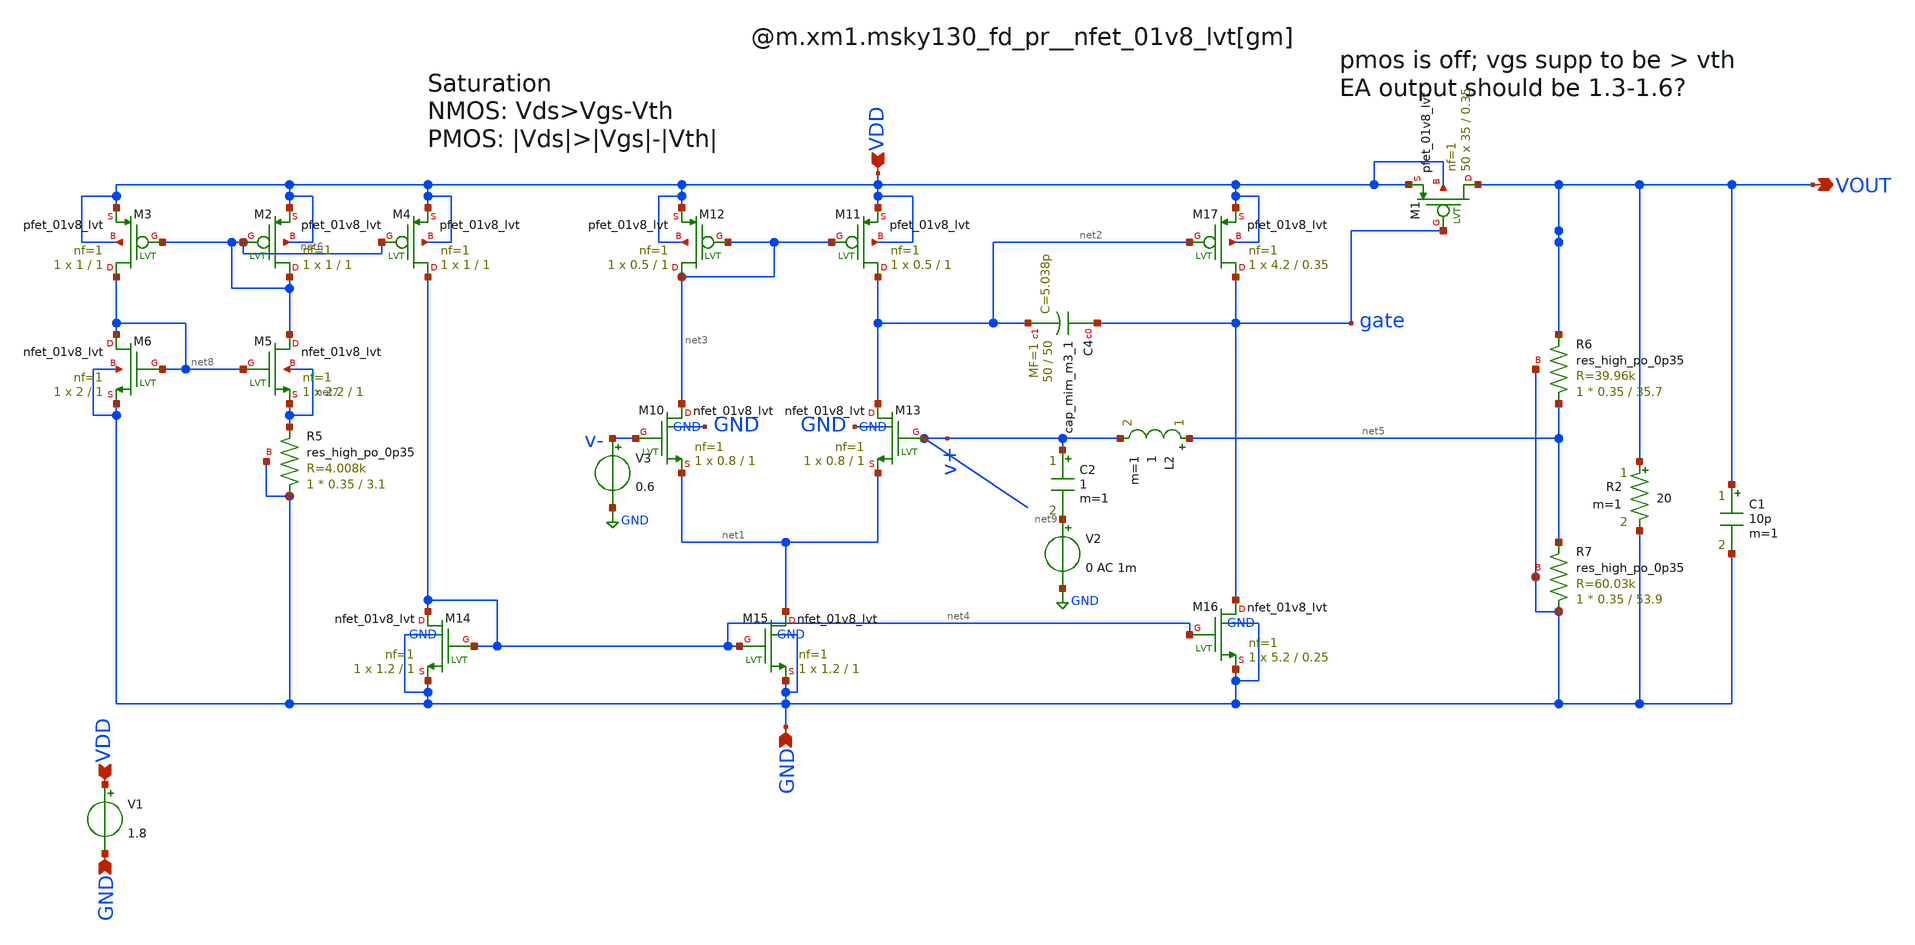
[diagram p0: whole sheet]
** sch_path: xschem/testbenches/FreqResponse-v4.sch
**.subckt FreqResponse-v4 VDD VOUT GND VDD GND
*.ipin VDD
*.opin VOUT
*.ipin GND
*.ipin VDD
*.ipin GND
V3 v- GND 0.6
XM10 net3 v- net1 GND sky130_fd_pr__nfet_01v8_lvt L=1 W=0.8 nf=1 ad='int((1 + 1)/2) * 0.8 / 1 * 0.29'
+ as='int((1 + 2)/2) * 0.8 / 1 * 0.29' pd='2*int((1 + 1)/2) * (0.8 / 1 + 0.29)' ps='2*int((1 + 2)/2) * (0.8 / 1 + 0.29)'
+ nrd='0.29 / 0.8 ' nrs='0.29 / 0.8 ' sa=0 sb=0 sd=0 mult=1 m=1
XM11 net2 net3 VDD VDD sky130_fd_pr__pfet_01v8_lvt L=1 W=0.5 nf=1 ad='int((1 + 1)/2) * 0.5 / 1 * 0.29'
+ as='int((1 + 2)/2) * 0.5 / 1 * 0.29' pd='2*int((1 + 1)/2) * (0.5 / 1 + 0.29)' ps='2*int((1 + 2)/2) * (0.5 / 1 + 0.29)'
+ nrd='0.29 / 0.5 ' nrs='0.29 / 0.5 ' sa=0 sb=0 sd=0 mult=1 m=1
XM12 net3 net3 VDD VDD sky130_fd_pr__pfet_01v8_lvt L=1 W=0.5 nf=1 ad='int((1 + 1)/2) * 0.5 / 1 * 0.29'
+ as='int((1 + 2)/2) * 0.5 / 1 * 0.29' pd='2*int((1 + 1)/2) * (0.5 / 1 + 0.29)' ps='2*int((1 + 2)/2) * (0.5 / 1 + 0.29)'
+ nrd='0.29 / 0.5 ' nrs='0.29 / 0.5 ' sa=0 sb=0 sd=0 mult=1 m=1
XM13 net2 v+ net1 GND sky130_fd_pr__nfet_01v8_lvt L=1 W=0.8 nf=1 ad='int((1 + 1)/2) * 0.8 / 1 * 0.29'
+ as='int((1 + 2)/2) * 0.8 / 1 * 0.29' pd='2*int((1 + 1)/2) * (0.8 / 1 + 0.29)' ps='2*int((1 + 2)/2) * (0.8 / 1 + 0.29)'
+ nrd='0.29 / 0.8 ' nrs='0.29 / 0.8 ' sa=0 sb=0 sd=0 mult=1 m=1
XM14 net4 net4 GND GND sky130_fd_pr__nfet_01v8_lvt L=1 W=1.2 nf=1 ad='int((1 + 1)/2) * 1.2 / 1 * 0.29'
+ as='int((1 + 2)/2) * 1.2 / 1 * 0.29' pd='2*int((1 + 1)/2) * (1.2 / 1 + 0.29)' ps='2*int((1 + 2)/2) * (1.2 / 1 + 0.29)'
+ nrd='0.29 / 1.2 ' nrs='0.29 / 1.2 ' sa=0 sb=0 sd=0 mult=1 m=1
XM15 net1 net4 GND GND sky130_fd_pr__nfet_01v8_lvt L=1 W=1.2 nf=1 ad='int((1 + 1)/2) * 1.2 / 1 * 0.29'
+ as='int((1 + 2)/2) * 1.2 / 1 * 0.29' pd='2*int((1 + 1)/2) * (1.2 / 1 + 0.29)' ps='2*int((1 + 2)/2) * (1.2 / 1 + 0.29)'
+ nrd='0.29 / 1.2 ' nrs='0.29 / 1.2 ' sa=0 sb=0 sd=0 mult=1 m=1
XM16 gate net4 GND GND sky130_fd_pr__nfet_01v8_lvt L=0.25 W=5.2 nf=1 ad='int((1 + 1)/2) * 5.2 / 1 * 0.29'
+ as='int((1 + 2)/2) * 5.2 / 1 * 0.29' pd='2*int((1 + 1)/2) * (5.2 / 1 + 0.29)' ps='2*int((1 + 2)/2) * (5.2 / 1 + 0.29)'
+ nrd='0.29 / 5.2 ' nrs='0.29 / 5.2 ' sa=0 sb=0 sd=0 mult=1 m=1
XM17 gate net2 VDD VDD sky130_fd_pr__pfet_01v8_lvt L=0.35 W=4.2 nf=1 ad='int((1 + 1)/2) * 4.2 / 1 * 0.29'
+ as='int((1 + 2)/2) * 4.2 / 1 * 0.29' pd='2*int((1 + 1)/2) * (4.2 / 1 + 0.29)' ps='2*int((1 + 2)/2) * (4.2 / 1 + 0.29)'
+ nrd='0.29 / 4.2 ' nrs='0.29 / 4.2 ' sa=0 sb=0 sd=0 mult=1 m=1
XM1 VOUT gate VDD VDD sky130_fd_pr__pfet_01v8_lvt L=0.35 W=35 nf=1 ad='int((1 + 1)/2) * 35 / 1 * 0.29'
+ as='int((1 + 2)/2) * 35 / 1 * 0.29' pd='2*int((1 + 1)/2) * (35 / 1 + 0.29)' ps='2*int((1 + 2)/2) * (35 / 1 + 0.29)'
+ nrd='0.29 / 35 ' nrs='0.29 / 35 ' sa=0 sb=0 sd=0 mult=50 m=50
V1 VDD GND 1.8
V2 net9 GND 0 AC 1m
R2 VOUT GND 20 m=1
C1 VOUT GND 10p m=1
XM2 net6 net6 VDD VDD sky130_fd_pr__pfet_01v8_lvt L=1 W=1 nf=1 ad='int((1 + 1)/2) * 1 / 1 * 0.29' as='int((1 + 2)/2) * 1 / 1 * 0.29'
+ pd='2*int((1 + 1)/2) * (1 / 1 + 0.29)' ps='2*int((1 + 2)/2) * (1 / 1 + 0.29)' nrd='0.29 / 1 ' nrs='0.29 / 1 '
+ sa=0 sb=0 sd=0 mult=1 m=1
XM3 net8 net6 VDD VDD sky130_fd_pr__pfet_01v8_lvt L=1 W=1 nf=1 ad='int((1 + 1)/2) * 1 / 1 * 0.29' as='int((1 + 2)/2) * 1 / 1 * 0.29'
+ pd='2*int((1 + 1)/2) * (1 / 1 + 0.29)' ps='2*int((1 + 2)/2) * (1 / 1 + 0.29)' nrd='0.29 / 1 ' nrs='0.29 / 1 '
+ sa=0 sb=0 sd=0 mult=1 m=1
XM4 net4 net6 VDD VDD sky130_fd_pr__pfet_01v8_lvt L=1 W=1 nf=1 ad='int((1 + 1)/2) * 1 / 1 * 0.29' as='int((1 + 2)/2) * 1 / 1 * 0.29'
+ pd='2*int((1 + 1)/2) * (1 / 1 + 0.29)' ps='2*int((1 + 2)/2) * (1 / 1 + 0.29)' nrd='0.29 / 1 ' nrs='0.29 / 1 '
+ sa=0 sb=0 sd=0 mult=1 m=1
XM5 net6 net8 net7 net7 sky130_fd_pr__nfet_01v8_lvt L=1 W=2.2 nf=1 ad='int((1 + 1)/2) * 2.2 / 1 * 0.29'
+ as='int((1 + 2)/2) * 2.2 / 1 * 0.29' pd='2*int((1 + 1)/2) * (2.2 / 1 + 0.29)' ps='2*int((1 + 2)/2) * (2.2 / 1 + 0.29)'
+ nrd='0.29 / 2.2 ' nrs='0.29 / 2.2 ' sa=0 sb=0 sd=0 mult=1 m=1
XM6 net8 net8 GND GND sky130_fd_pr__nfet_01v8_lvt L=1 W=2 nf=1 ad='int((1 + 1)/2) * 2 / 1 * 0.29' as='int((1 + 2)/2) * 2 / 1 * 0.29'
+ pd='2*int((1 + 1)/2) * (2 / 1 + 0.29)' ps='2*int((1 + 2)/2) * (2 / 1 + 0.29)' nrd='0.29 / 2 ' nrs='0.29 / 2 '
+ sa=0 sb=0 sd=0 mult=1 m=1
XR5 GND net7 GND sky130_fd_pr__res_high_po_0p35 L=3.1 mult=1 m=1
XR6 net5 VOUT GND sky130_fd_pr__res_high_po_0p35 L=35.7 mult=1 m=1
XR7 GND net5 GND sky130_fd_pr__res_high_po_0p35 L=53.9 mult=1 m=1
XC4 gate net2 sky130_fd_pr__cap_mim_m3_1 W=50 L=50 MF=1 m=1
L2 net5 v+ 1 m=1
C2 v+ net9 1 m=1
**** begin user architecture code



.lib /usr/local/share/pdk/sky130A/libs.tech/ngspice/sky130.lib.spice tt
.ac dec 20 1 1e12
*.tran 5u 5m

.control
run
print 1/@m.xm1.msky130_fd_pr__pfet_01v8_lvt[gds]
*plot vout
plot db(vout/v(v+))
plot 180*cph(vout)/pi+360
.endc


**** end user architecture code
**.ends
.GLOBAL GND
.end
